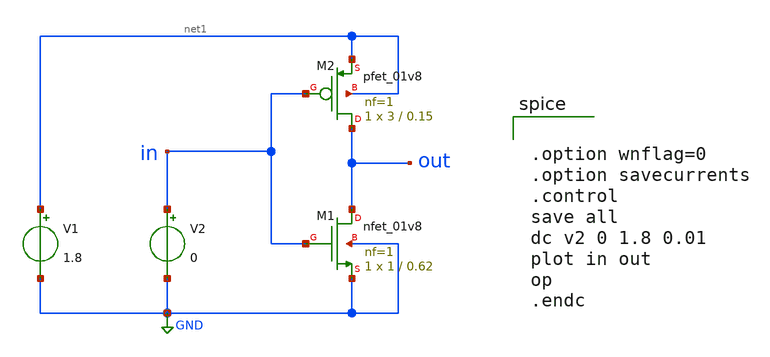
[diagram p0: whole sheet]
** sch_path: Inverter_Assignment_1.sch
**.subckt Inverter_Assignment_1
V1 net1 GND 1.8
V2 in GND 0
XM1 out in GND GND sky130_fd_pr__nfet_01v8 L=0.62 W=1 nf=1 ad='int((nf+1)/2) * W/nf * 0.29' as='int((nf+2)/2) * W/nf * 0.29'
+ pd='2*int((nf+1)/2) * (W/nf + 0.29)' ps='2*int((nf+2)/2) * (W/nf + 0.29)' nrd='0.29 / W' nrs='0.29 / W'
+ sa=0 sb=0 sd=0 mult=1 m=1
XM2 out in net1 net1 sky130_fd_pr__pfet_01v8 L=0.15 W=3 nf=1 ad='int((nf+1)/2) * W/nf * 0.29' as='int((nf+2)/2) * W/nf * 0.29'
+ pd='2*int((nf+1)/2) * (W/nf + 0.29)' ps='2*int((nf+2)/2) * (W/nf + 0.29)' nrd='0.29 / W' nrs='0.29 / W'
+ sa=0 sb=0 sd=0 mult=1 m=1
**** begin user architecture code
 .lib $::SKYWATER_MODELS/sky130.lib.spice tt

.param mc_mm_switch=0
.param mc_pr_switch=1



.option wnflag=0
.option savecurrents
.control
save all
dc v2 0 1.8 0.01
plot in out
op
.endc


**** end user architecture code
**.ends
.GLOBAL GND
.end
